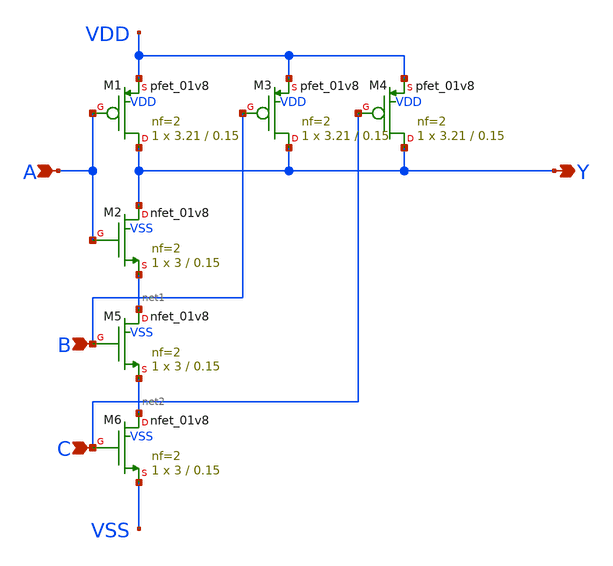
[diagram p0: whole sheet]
** sch_path: design/xschem/NAND/nand3.sch
**.subckt nand3 A Y B C
*.ipin A
*.opin Y
*.ipin B
*.ipin C
XM1 Y A VDD VDD sky130_fd_pr__pfet_01v8 L=0.15 W=3.21 nf=2 ad='int((nf+1)/2) * W/nf * 0.29' as='int((nf+2)/2) * W/nf * 0.29'
+ pd='2*int((nf+1)/2) * (W/nf + 0.29)' ps='2*int((nf+2)/2) * (W/nf + 0.29)' nrd='0.29 / W' nrs='0.29 / W'
+ sa=0 sb=0 sd=0 mult=1 m=1
XM2 Y A net1 VSS sky130_fd_pr__nfet_01v8 L=0.15 W=3 nf=2 ad='int((nf+1)/2) * W/nf * 0.29' as='int((nf+2)/2) * W/nf * 0.29'
+ pd='2*int((nf+1)/2) * (W/nf + 0.29)' ps='2*int((nf+2)/2) * (W/nf + 0.29)' nrd='0.29 / W' nrs='0.29 / W'
+ sa=0 sb=0 sd=0 mult=1 m=1
XM3 Y B VDD VDD sky130_fd_pr__pfet_01v8 L=0.15 W=3.21 nf=2 ad='int((nf+1)/2) * W/nf * 0.29' as='int((nf+2)/2) * W/nf * 0.29'
+ pd='2*int((nf+1)/2) * (W/nf + 0.29)' ps='2*int((nf+2)/2) * (W/nf + 0.29)' nrd='0.29 / W' nrs='0.29 / W'
+ sa=0 sb=0 sd=0 mult=1 m=1
XM4 Y C VDD VDD sky130_fd_pr__pfet_01v8 L=0.15 W=3.21 nf=2 ad='int((nf+1)/2) * W/nf * 0.29' as='int((nf+2)/2) * W/nf * 0.29'
+ pd='2*int((nf+1)/2) * (W/nf + 0.29)' ps='2*int((nf+2)/2) * (W/nf + 0.29)' nrd='0.29 / W' nrs='0.29 / W'
+ sa=0 sb=0 sd=0 mult=1 m=1
XM5 net1 B net2 VSS sky130_fd_pr__nfet_01v8 L=0.15 W=3 nf=2 ad='int((nf+1)/2) * W/nf * 0.29' as='int((nf+2)/2) * W/nf * 0.29'
+ pd='2*int((nf+1)/2) * (W/nf + 0.29)' ps='2*int((nf+2)/2) * (W/nf + 0.29)' nrd='0.29 / W' nrs='0.29 / W'
+ sa=0 sb=0 sd=0 mult=1 m=1
XM6 net2 C VSS VSS sky130_fd_pr__nfet_01v8 L=0.15 W=3 nf=2 ad='int((nf+1)/2) * W/nf * 0.29' as='int((nf+2)/2) * W/nf * 0.29'
+ pd='2*int((nf+1)/2) * (W/nf + 0.29)' ps='2*int((nf+2)/2) * (W/nf + 0.29)' nrd='0.29 / W' nrs='0.29 / W'
+ sa=0 sb=0 sd=0 mult=1 m=1
**.ends
.end
